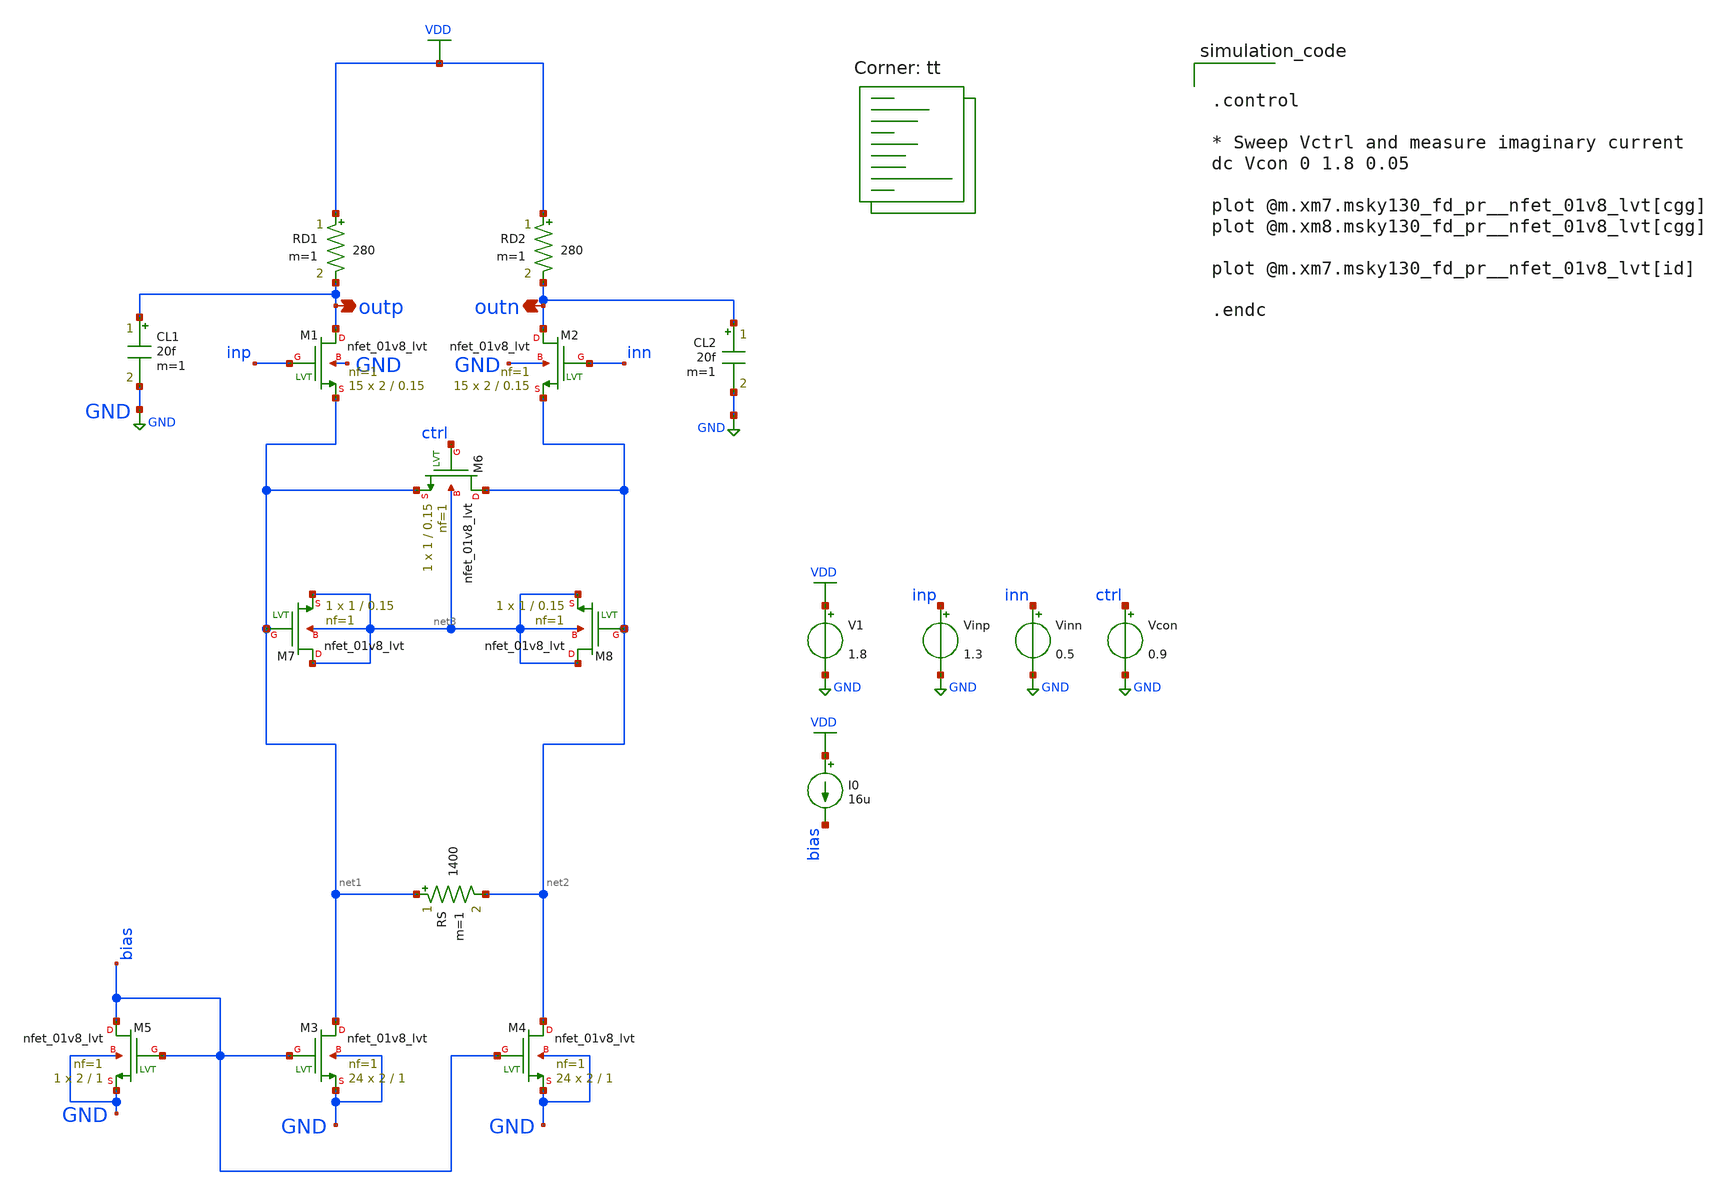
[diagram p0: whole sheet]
** sch_path: CTLE/ctle_sym_adaptive_cap.sch
**.subckt ctle_sym_adaptive_cap outp outn
*.opin outp
*.opin outn
XM1 outp inp net1 GND sky130_fd_pr__nfet_01v8_lvt L=0.15 W=2 nf=1 ad='int((nf+1)/2) * W/nf * 0.29' as='int((nf+2)/2) * W/nf * 0.29'
+ pd='2*int((nf+1)/2) * (W/nf + 0.29)' ps='2*int((nf+2)/2) * (W/nf + 0.29)' nrd='0.29 / W' nrs='0.29 / W'
+ sa=0 sb=0 sd=0 mult=15 m=15
XM2 outn inn net2 GND sky130_fd_pr__nfet_01v8_lvt L=0.15 W=2 nf=1 ad='int((nf+1)/2) * W/nf * 0.29' as='int((nf+2)/2) * W/nf * 0.29'
+ pd='2*int((nf+1)/2) * (W/nf + 0.29)' ps='2*int((nf+2)/2) * (W/nf + 0.29)' nrd='0.29 / W' nrs='0.29 / W'
+ sa=0 sb=0 sd=0 mult=15 m=15
XM3 net1 bias GND GND sky130_fd_pr__nfet_01v8_lvt L=1 W=2 nf=1 ad='int((nf+1)/2) * W/nf * 0.29' as='int((nf+2)/2) * W/nf * 0.29'
+ pd='2*int((nf+1)/2) * (W/nf + 0.29)' ps='2*int((nf+2)/2) * (W/nf + 0.29)' nrd='0.29 / W' nrs='0.29 / W'
+ sa=0 sb=0 sd=0 mult=24 m=24
XM4 net2 bias GND GND sky130_fd_pr__nfet_01v8_lvt L=1 W=2 nf=1 ad='int((nf+1)/2) * W/nf * 0.29' as='int((nf+2)/2) * W/nf * 0.29'
+ pd='2*int((nf+1)/2) * (W/nf + 0.29)' ps='2*int((nf+2)/2) * (W/nf + 0.29)' nrd='0.29 / W' nrs='0.29 / W'
+ sa=0 sb=0 sd=0 mult=24 m=24
XM5 bias bias GND GND sky130_fd_pr__nfet_01v8_lvt L=1 W=2 nf=1 ad='int((nf+1)/2) * W/nf * 0.29' as='int((nf+2)/2) * W/nf * 0.29'
+ pd='2*int((nf+1)/2) * (W/nf + 0.29)' ps='2*int((nf+2)/2) * (W/nf + 0.29)' nrd='0.29 / W' nrs='0.29 / W'
+ sa=0 sb=0 sd=0 mult=1 m=1
RD1 VDD outp 280 m=1
RD2 VDD outn 280 m=1
RS net1 net2 1400 m=1
CL1 outp GND 20f m=1
CL2 outn GND 20f m=1
XM6 net2 ctrl net1 net3 sky130_fd_pr__nfet_01v8_lvt L=0.15 W=1 nf=1 ad='int((nf+1)/2) * W/nf * 0.29'
+ as='int((nf+2)/2) * W/nf * 0.29' pd='2*int((nf+1)/2) * (W/nf + 0.29)' ps='2*int((nf+2)/2) * (W/nf + 0.29)'
+ nrd='0.29 / W' nrs='0.29 / W' sa=0 sb=0 sd=0 mult=1 m=1
XM7 net3 net1 net3 net3 sky130_fd_pr__nfet_01v8_lvt L=0.15 W=1 nf=1 ad='int((nf+1)/2) * W/nf * 0.29'
+ as='int((nf+2)/2) * W/nf * 0.29' pd='2*int((nf+1)/2) * (W/nf + 0.29)' ps='2*int((nf+2)/2) * (W/nf + 0.29)'
+ nrd='0.29 / W' nrs='0.29 / W' sa=0 sb=0 sd=0 mult=1 m=1
XM8 net3 net2 net3 net3 sky130_fd_pr__nfet_01v8_lvt L=0.15 W=1 nf=1 ad='int((nf+1)/2) * W/nf * 0.29'
+ as='int((nf+2)/2) * W/nf * 0.29' pd='2*int((nf+1)/2) * (W/nf + 0.29)' ps='2*int((nf+2)/2) * (W/nf + 0.29)'
+ nrd='0.29 / W' nrs='0.29 / W' sa=0 sb=0 sd=0 mult=1 m=1
V1 VDD GND 1.8
Vinp inp GND 1.3
Vinn inn GND 0.5
Vcon ctrl GND 0.9
I0 VDD bias 16u
**** begin user architecture code
.lib $::SKYWATER_MODELS/sky130.lib.spice tt


.control

* Sweep Vctrl and measure imaginary current
dc Vcon 0 1.8 0.05

plot @m.xm7.msky130_fd_pr__nfet_01v8_lvt[cgg]
plot @m.xm8.msky130_fd_pr__nfet_01v8_lvt[cgg]

plot @m.xm7.msky130_fd_pr__nfet_01v8_lvt[id]

.endc


**** end user architecture code
**.ends
.GLOBAL GND
.GLOBAL VDD
.end
